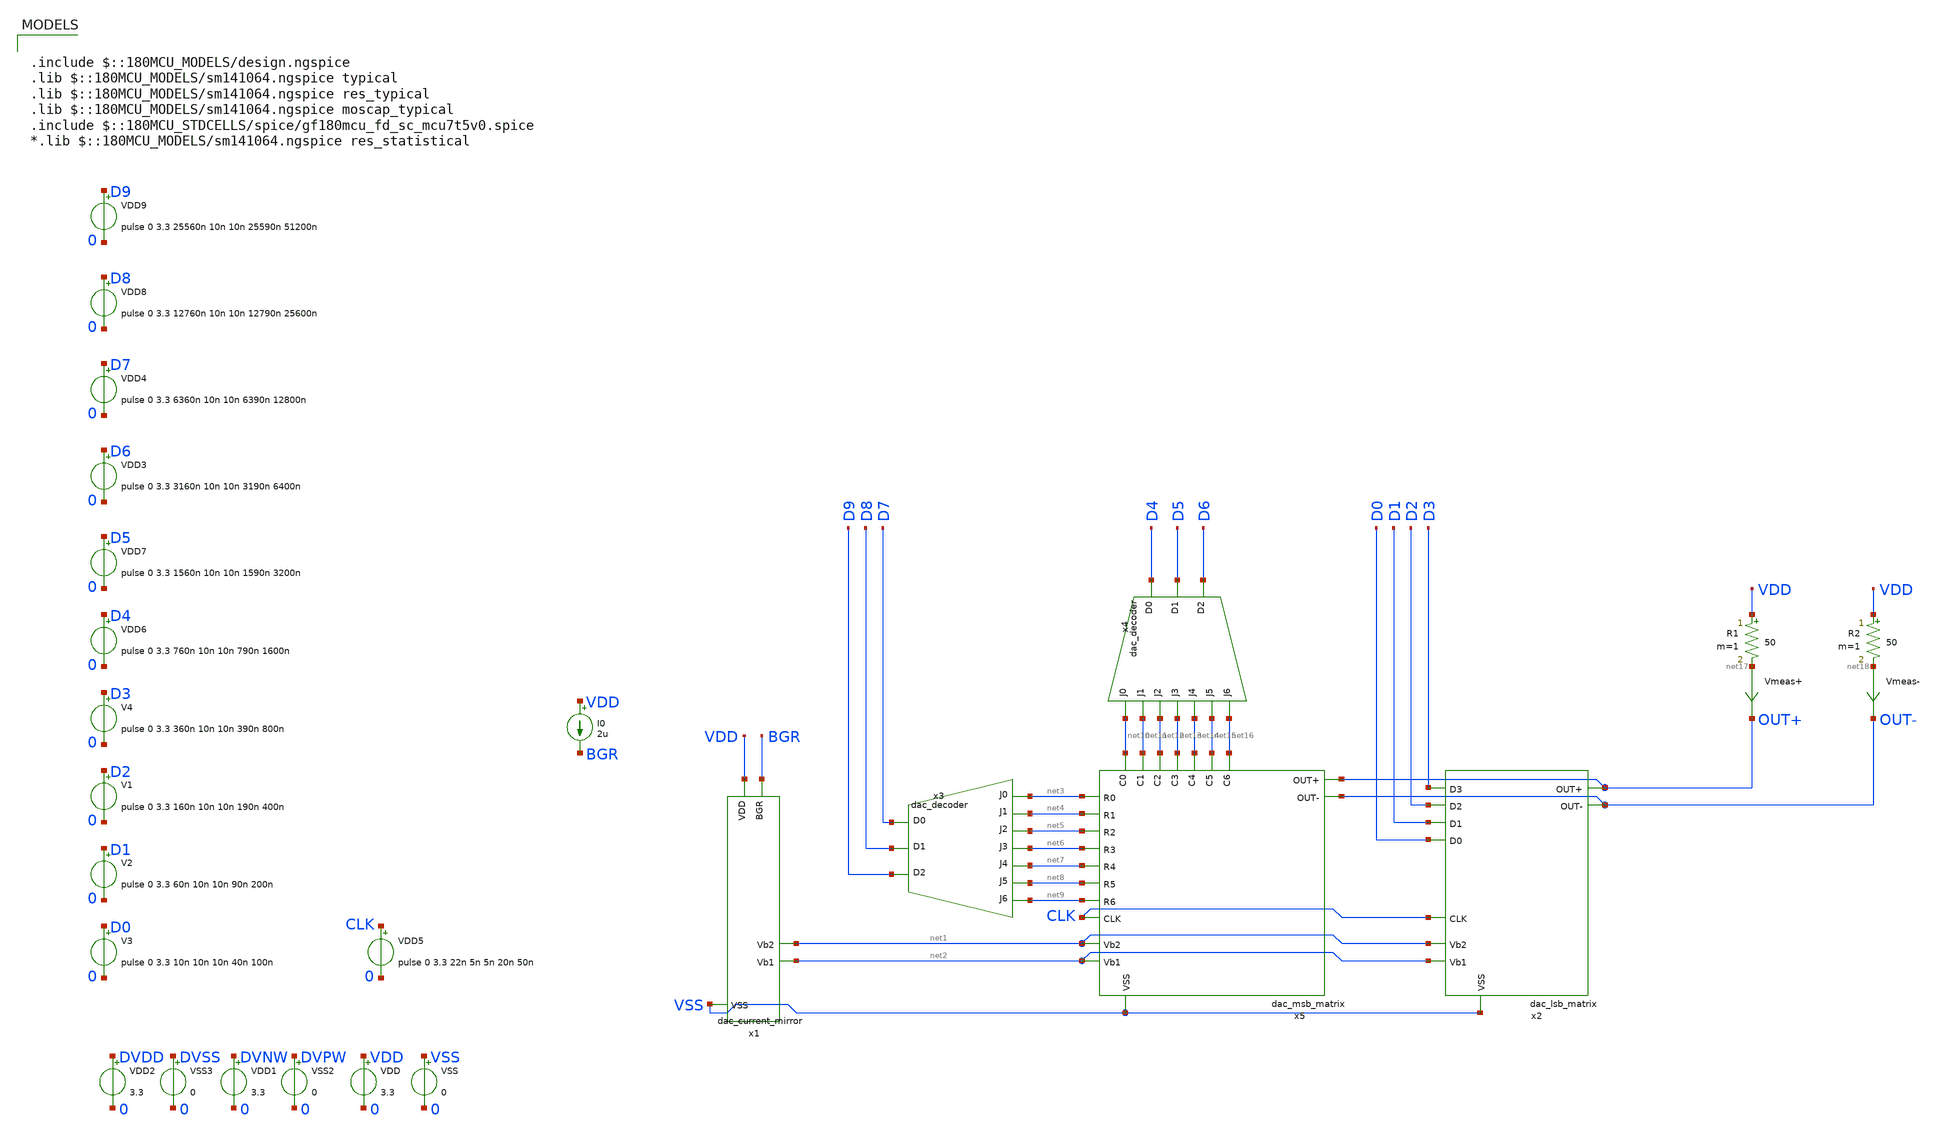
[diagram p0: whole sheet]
** sch_path: xschem/test_dac_top.sch
**.subckt test_dac_top
x3 net9 net8 net7 net6 net5 net4 D9 D8 D7 net3 DVDD DVNW DVPW DVSS dac_decoder
x4 net16 net15 net14 net13 net12 net11 D6 D5 D4 net10 DVDD DVNW DVPW DVSS dac_decoder
VDD6 D4 0 pulse 0 3.3 760n 10n 10n 790n 1600n
VDD7 D5 0 pulse 0 3.3 1560n 10n 10n 1590n 3200n
VDD VDD 0 3.3
VSS VSS 0 0
VDD1 DVNW 0 3.3
VSS2 DVPW 0 0
VDD2 DVDD 0 3.3
VSS3 DVSS 0 0
V1 D2 0 pulse 0 3.3 160n 10n 10n 190n 400n
V2 D1 0 pulse 0 3.3 60n 10n 10n 90n 200n
V3 D0 0 pulse 0 3.3 10n 10n 10n 40n 100n
V4 D3 0 pulse 0 3.3 360n 10n 10n 390n 800n
VDD5 CLK 0 pulse 0 3.3 22n 5n 5n 20n 50n
VDD3 D6 0 pulse 0 3.3 3160n 10n 10n 3190n 6400n
VDD4 D7 0 pulse 0 3.3 6360n 10n 10n 6390n 12800n
I0 VDD BGR 2u
VDD8 D8 0 pulse 0 3.3 12760n 10n 10n 12790n 25600n
VDD9 D9 0 pulse 0 3.3 25560n 10n 10n 25590n 51200n
R1 VDD net17 50 m=1
R2 VDD net18 50 m=1
Vmeas+ net17 OUT+ 0
.save i(vmeas+)
Vmeas- net18 OUT- 0
.save i(vmeas-)
x1 VDD BGR net1 net2 VSS dac_current_mirror
x2 D2 D3 D1 D0 OUT+ OUT- CLK net1 net2 VSS DVDD DVNW DVPW DVSS dac_lsb_matrix
x5 net15 net11 net14 net13 net12 net10 net16 net3 CLK OUT+ OUT- net1 net2 net4 net5 net6 net7 net8
+ net9 VSS DVDD DVNW DVPW DVSS dac_msb_matrix
**** begin user architecture code

.include $::180MCU_MODELS/design.ngspice
.lib $::180MCU_MODELS/sm141064.ngspice typical
.lib $::180MCU_MODELS/sm141064.ngspice res_typical
.lib $::180MCU_MODELS/sm141064.ngspice moscap_typical
.include $::180MCU_STDCELLS/spice/gf180mcu_fd_sc_mcu7t5v0.spice
*.lib $::180MCU_MODELS/sm141064.ngspice res_statistical





.control
	tran 5n 51200n
	plot v(D0) v(D1) v(D2) v(D3) v(D4) v(D5) v(CLK)
	plot i(Vmeas+) i(Vmeas-)
	write test_dac_top.raw
.endc
.save all




**** end user architecture code
**.ends
.end
